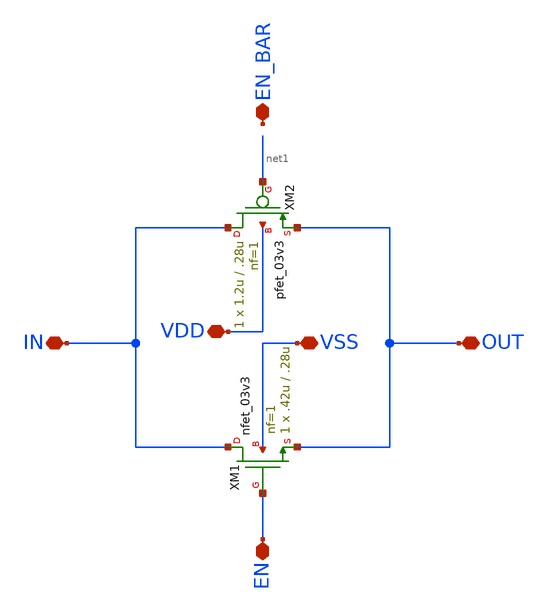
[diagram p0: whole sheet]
** sch_path: designs/libs/old_files/etj_test_def/tgate.sch
**.subckt tgate IN OUT EN EN_BAR VSS VDD
*.iopin IN
*.iopin OUT
*.iopin EN
*.iopin EN_BAR
*.iopin VSS
*.iopin VDD
XM1 IN EN OUT VSS nfet_03v3 L=.28u W=.42u nf=1 ad='int((nf+1)/2) * W/nf * 0.18u' as='int((nf+2)/2) * W/nf * 0.18u'
+ pd='2*int((nf+1)/2) * (W/nf + 0.18u)' ps='2*int((nf+2)/2) * (W/nf + 0.18u)' nrd='0.18u / W' nrs='0.18u / W'
+ sa=0 sb=0 sd=0 m=1
XM2 IN net1 OUT VDD pfet_03v3 L=.28u W=1.2u nf=1 ad='int((nf+1)/2) * W/nf * 0.18u' as='int((nf+2)/2) * W/nf * 0.18u'
+ pd='2*int((nf+1)/2) * (W/nf + 0.18u)' ps='2*int((nf+2)/2) * (W/nf + 0.18u)' nrd='0.18u / W' nrs='0.18u / W'
+ sa=0 sb=0 sd=0 m=1
**.ends
.end
